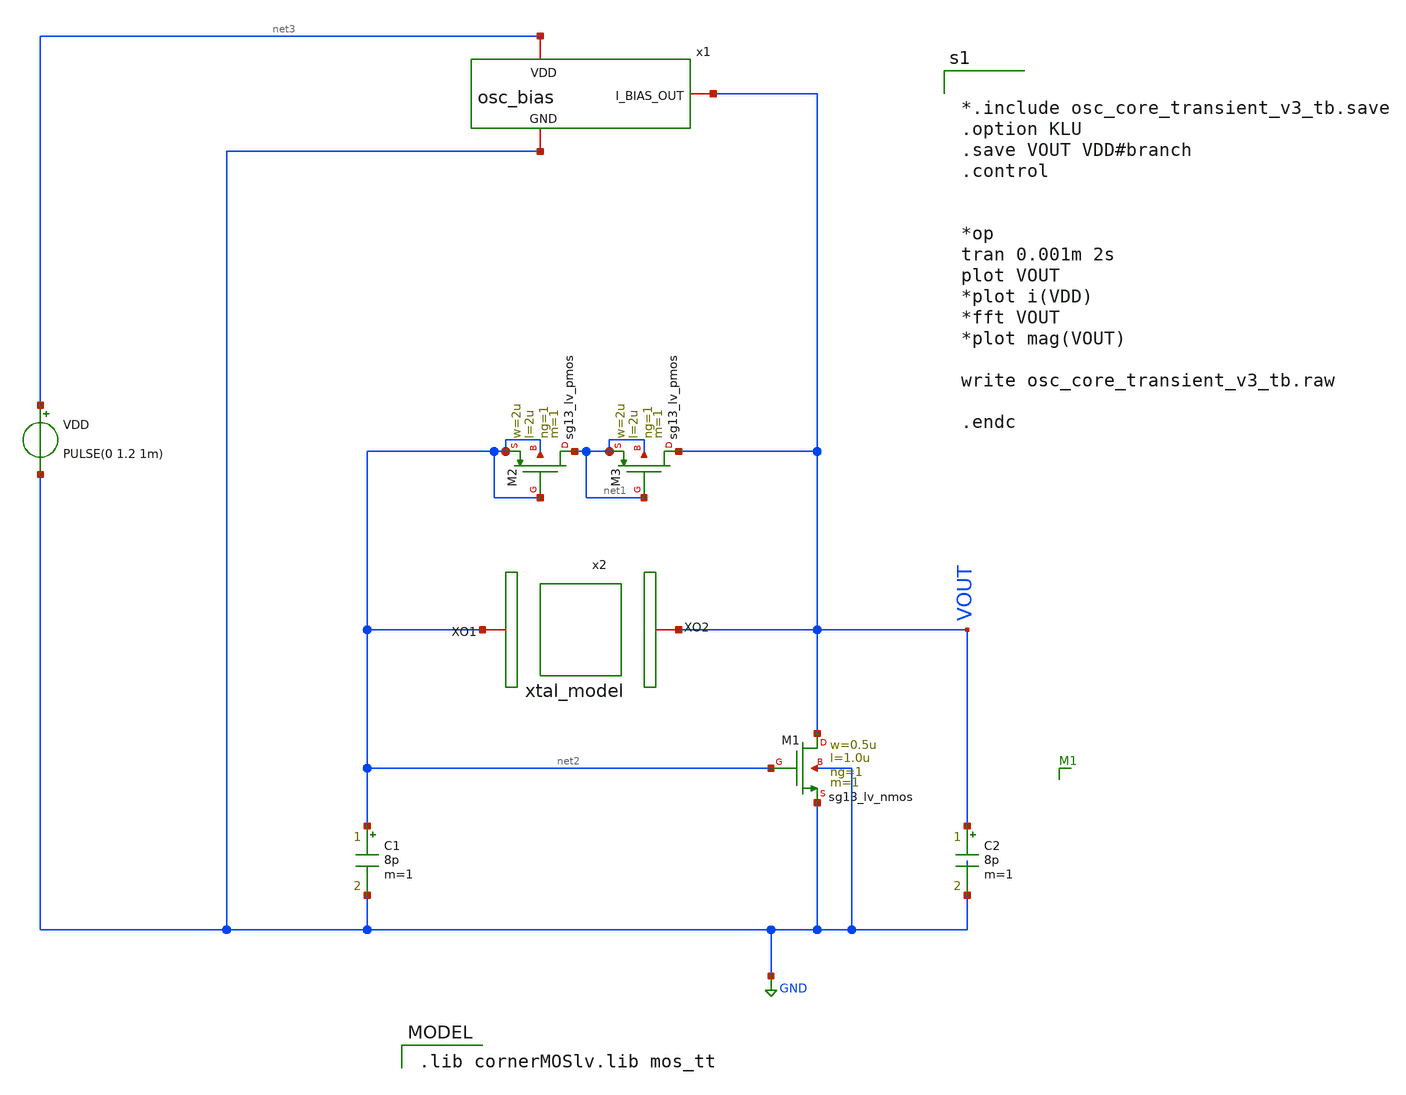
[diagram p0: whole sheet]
** sch_path: osc_core_transient_v3_tb.sch
**.subckt osc_core_transient_v3_tb
XM1 VOUT net2 GND GND sg13_lv_nmos w=0.5u l=1.0u ng=1 m=1 mm_ok=1
C1 net2 GND 8p m=1
C2 VOUT GND 8p m=1
VDD net3 GND PULSE(0 1.2 1m)
XM2 net1 net2 net2 net2 sg13_lv_pmos w=2u l=2u ng=1 m=1 mm_ok=1
XM3 VOUT net1 net1 net1 sg13_lv_pmos w=2u l=2u ng=1 m=1 mm_ok=1
x1 net3 VOUT GND osc_bias
x2 net2 VOUT xtal_model
**** begin user architecture code


*.include osc_core_transient_v3_tb.save
.option KLU
.save VOUT VDD#branch
.control


*op
tran 0.001m 2s
plot VOUT
*plot i(VDD)
*fft VOUT
*plot mag(VOUT)

write osc_core_transient_v3_tb.raw

.endc


 .lib cornerMOSlv.lib mos_tt

**** end user architecture code
**.ends

* expanding   symbol:  /foss/designs/xtal/osc_bias.sym # of pins=3
** sym_path: osc_bias.sym
** sch_path: osc_bias.sch
.subckt osc_bias VDD I_BIAS_OUT GND
*.iopin VDD
*.iopin GND
*.iopin I_BIAS_OUT
XM1 vp_bias vp_bias VDD VDD sg13_lv_pmos w=0.5u l=10u ng=1 m=1 mm_ok=1
XM3 vp_bias vp_bias net2 net1 sg13_lv_nmos w=0.25u l=15u ng=1 m=1 mm_ok=1
XM4 net2 net2 net3 net1 sg13_lv_nmos w=0.25u l=15u ng=1 m=1 mm_ok=1
XM5 net3 net3 net1 net1 sg13_lv_nmos w=0.25u l=15u ng=1 m=1 mm_ok=1
XM2 I_BIAS_OUT vp_bias VDD VDD sg13_lv_pmos w=0.5u l=10u ng=1 m=1 mm_ok=1
Vmeas_ref_path net1 GND 0
.save i(vmeas_ref_path)
.ends


* expanding   symbol:  /foss/designs/xtal/xtal_model.sym # of pins=2
** sym_path: xtal_model.sym
** sch_path: xtal_model.sch
.subckt xtal_model XO1 XO2
*.iopin XO2
*.iopin XO1
R1 XO1 net1 1k m=1
Cm net1 net2 1p m=1
C0 XO1 XO2 1p m=1
Lm net2 XO2 1n m=1
.ends

.GLOBAL GND
.end
